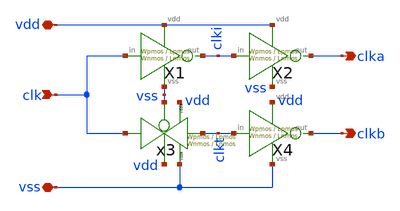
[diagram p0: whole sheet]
** sch_path: xschem/clkgen/comp_clks.sch
**.subckt comp_clks clk clka clkb vdd vss
*.ipin clk
*.opin clka
*.opin clkb
*.iopin vdd
*.iopin vss
X1 clk clki vdd vss inv Wpmos=Wpmos Lpmos=Lpmos Wnmos=Wnmos Lnmos=Lnmos
X2 clki clka vdd vss inv Wpmos=Wpmos Lpmos=Lpmos Wnmos=Wnmos Lnmos=Lnmos
X4 clkt clkb vdd vss inv Wpmos=Wpmos Lpmos=Lpmos Wnmos=Wnmos Lnmos=Lnmos
x3 clk clkt vss vdd vdd vss tg Wpmos=Wpmos Lpmos=Lpmos Wnmos=Wnmos Lnmos=Lnmos
**.ends

* expanding   symbol:  xschem/inv/inv.sym # of pins=4
** sym_path: xschem/inv/inv.sym
** sch_path: xschem/inv/inv.sch
.subckt inv in out vdd vss  Wpmos=Wpmos Lpmos=Lpmos Wnmos=Wnmos Lnmos=Lnmos
*.ipin in
*.iopin out
*.iopin vdd
*.iopin vss
XM1 vss in out vss sky130_fd_pr__nfet_01v8 L=Lnmos W=Wnmos nf=1 ad='int((nf+1)/2) * W/nf * 0.29' as='int((nf+2)/2) * W/nf * 0.29'
+ pd='2*int((nf+1)/2) * (W/nf + 0.29)' ps='2*int((nf+2)/2) * (W/nf + 0.29)' nrd='0.29 / W' nrs='0.29 / W'
+ sa=0 sb=0 sd=0 mult=1 m=1
XM2 vdd in out vdd sky130_fd_pr__pfet_01v8 L=Lpmos W=Wpmos nf=1 ad='int((nf+1)/2) * W/nf * 0.29' as='int((nf+2)/2) * W/nf * 0.29'
+ pd='2*int((nf+1)/2) * (W/nf + 0.29)' ps='2*int((nf+2)/2) * (W/nf + 0.29)' nrd='0.29 / W' nrs='0.29 / W'
+ sa=0 sb=0 sd=0 mult=1 m=1
.ends


* expanding   symbol:  xschem/transmission_gate/tg.sym # of pins=6
** sym_path: xschem/transmission_gate/tg.sym
** sch_path: xschem/transmission_gate/tg.sch
.subckt tg in out ctrl_ ctrl vdda vssa  Wpmos=0.42 Lpmos=0.18 Wnmos=0.42 Lnmos=0.18
*.iopin in
*.iopin out
*.ipin ctrl_
*.ipin ctrl
*.ipin vdda
*.ipin vssa
XM1 out ctrl in vssa sky130_fd_pr__nfet_01v8 L=Lnmos W=Wnmos nf=1 ad='int((nf+1)/2) * W/nf * 0.29' as='int((nf+2)/2) * W/nf * 0.29'
+ pd='2*int((nf+1)/2) * (W/nf + 0.29)' ps='2*int((nf+2)/2) * (W/nf + 0.29)' nrd='0.29 / W' nrs='0.29 / W'
+ sa=0 sb=0 sd=0 mult=1 m=1
XM2 out ctrl_ in vdda sky130_fd_pr__pfet_01v8 L=Lpmos W=Wpmos nf=1 ad='int((nf+1)/2) * W/nf * 0.29' as='int((nf+2)/2) * W/nf * 0.29'
+ pd='2*int((nf+1)/2) * (W/nf + 0.29)' ps='2*int((nf+2)/2) * (W/nf + 0.29)' nrd='0.29 / W' nrs='0.29 / W'
+ sa=0 sb=0 sd=0 mult=2 m=2
.ends

.end
